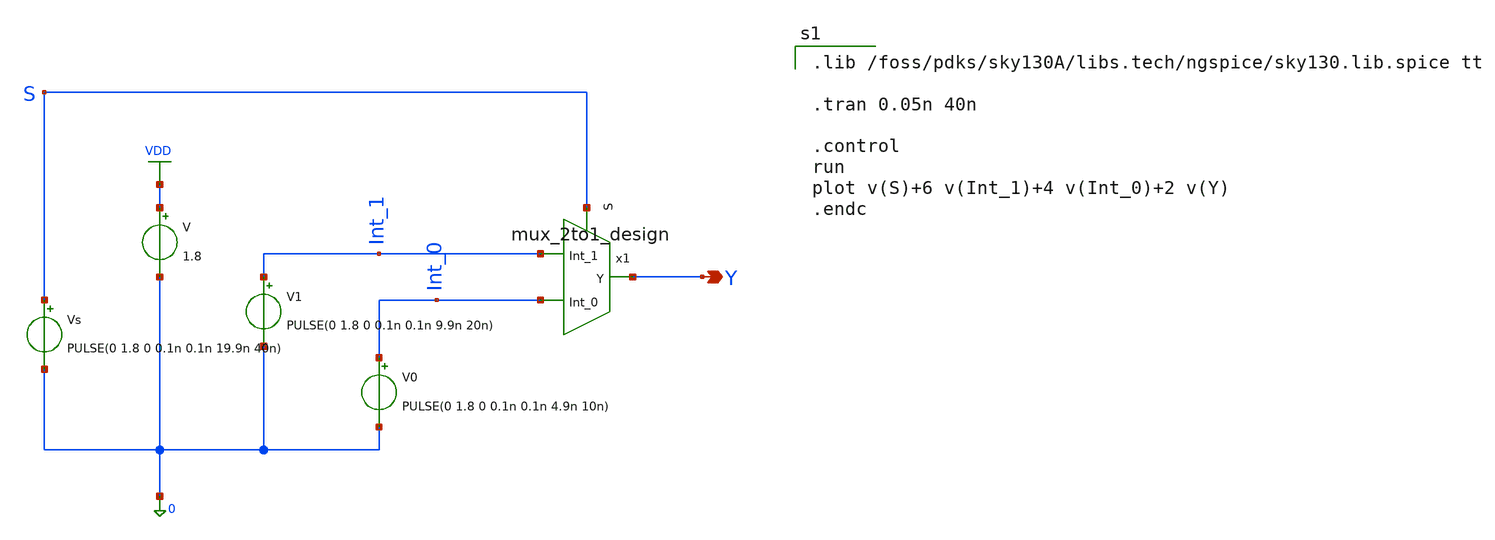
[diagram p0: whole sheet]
** sch_path: cells/full_adder_tg/xschem/tb_mux_2to1.sch
**.subckt tb_mux_2to1 Y
*.opin Y
V VDD 0 1.8
V1 Int_1 0 PULSE(0 1.8 0 0.1n 0.1n 9.9n 20n)
V0 Int_0 0 PULSE(0 1.8 0 0.1n 0.1n 4.9n 10n)
Vs S 0 PULSE(0 1.8 0 0.1n 0.1n 19.9n 40n)
x1 Int_1 Y S Int_0 mux_2to1_design
**** begin user architecture code

.lib /foss/pdks/sky130A/libs.tech/ngspice/sky130.lib.spice tt

.tran 0.05n 40n

.control
run
plot v(S)+6 v(Int_1)+4 v(Int_0)+2 v(Y)
.endc

**** end user architecture code
**.ends

* expanding   symbol:  ./mux_2to1_design.sym # of pins=4
** sym_path: cells/full_adder_tg/xschem/mux_2to1_design.sym
** sch_path: cells/full_adder_tg/xschem/mux_2to1_design.sch
.subckt mux_2to1_design Int_1 Y S Int_0
*.ipin Int_1
*.ipin Int_0
*.opin Y
*.ipin S
XMNmos_1 Y S Int_1 0 sky130_fd_pr__nfet_01v8 L=0.15 W=2 nf=1 ad='int((1 + 1)/2) * 2 / 1 * 0.29' as='int((1 + 2)/2) * 2 / 1 * 0.29'
+ pd='2*int((1 + 1)/2) * (2 / 1 + 0.29)' ps='2*int((1 + 2)/2) * (2 / 1 + 0.29)' nrd='0.29 / 2 ' nrs='0.29 / 2 '
+ sa=0 sb=0 sd=0 mult=1 m=1
XMPmos_1 Y net1 Int_1 VDD sky130_fd_pr__pfet_01v8 L=0.15 W=5 nf=1 ad='int((1 + 1)/2) * 5 / 1 * 0.29'
+ as='int((1 + 2)/2) * 5 / 1 * 0.29' pd='2*int((1 + 1)/2) * (5 / 1 + 0.29)' ps='2*int((1 + 2)/2) * (5 / 1 + 0.29)'
+ nrd='0.29 / 5 ' nrs='0.29 / 5 ' sa=0 sb=0 sd=0 mult=1 m=1
XMNmos_2 Y net1 Int_0 0 sky130_fd_pr__nfet_01v8 L=0.15 W=2 nf=1 ad='int((1 + 1)/2) * 2 / 1 * 0.29' as='int((1 + 2)/2) * 2 / 1 * 0.29'
+ pd='2*int((1 + 1)/2) * (2 / 1 + 0.29)' ps='2*int((1 + 2)/2) * (2 / 1 + 0.29)' nrd='0.29 / 2 ' nrs='0.29 / 2 '
+ sa=0 sb=0 sd=0 mult=1 m=1
XMPmos_2 Y S Int_0 VDD sky130_fd_pr__pfet_01v8 L=0.15 W=5 nf=1 ad='int((1 + 1)/2) * 5 / 1 * 0.29' as='int((1 + 2)/2) * 5 / 1 * 0.29'
+ pd='2*int((1 + 1)/2) * (5 / 1 + 0.29)' ps='2*int((1 + 2)/2) * (5 / 1 + 0.29)' nrd='0.29 / 5 ' nrs='0.29 / 5 '
+ sa=0 sb=0 sd=0 mult=1 m=1
x1 net1 S inveter_design
.ends


* expanding   symbol:  ./inveter_design.sym # of pins=2
** sym_path: cells/full_adder_tg/xschem/inveter_design.sym
** sch_path: cells/full_adder_tg/xschem/inveter_design.sch
.subckt inveter_design Out In
*.ipin In
*.opin Out
XMNMOS Out In 0 0 sky130_fd_pr__nfet_01v8 L=0.15 W=2 nf=1 ad='int((1 + 1)/2) * 2 / 1 * 0.29' as='int((1 + 2)/2) * 2 / 1 * 0.29'
+ pd='2*int((1 + 1)/2) * (2 / 1 + 0.29)' ps='2*int((1 + 2)/2) * (2 / 1 + 0.29)' nrd='0.29 / 2 ' nrs='0.29 / 2 '
+ sa=0 sb=0 sd=0 mult=1 m=1
XMPMOS Out In VDD VDD sky130_fd_pr__pfet_01v8 L=0.15 W=5 nf=1 ad='int((1 + 1)/2) * 5 / 1 * 0.29' as='int((1 + 2)/2) * 5 / 1 * 0.29'
+ pd='2*int((1 + 1)/2) * (5 / 1 + 0.29)' ps='2*int((1 + 2)/2) * (5 / 1 + 0.29)' nrd='0.29 / 5 ' nrs='0.29 / 5 '
+ sa=0 sb=0 sd=0 mult=1 m=1
.ends

.GLOBAL VDD
.end
